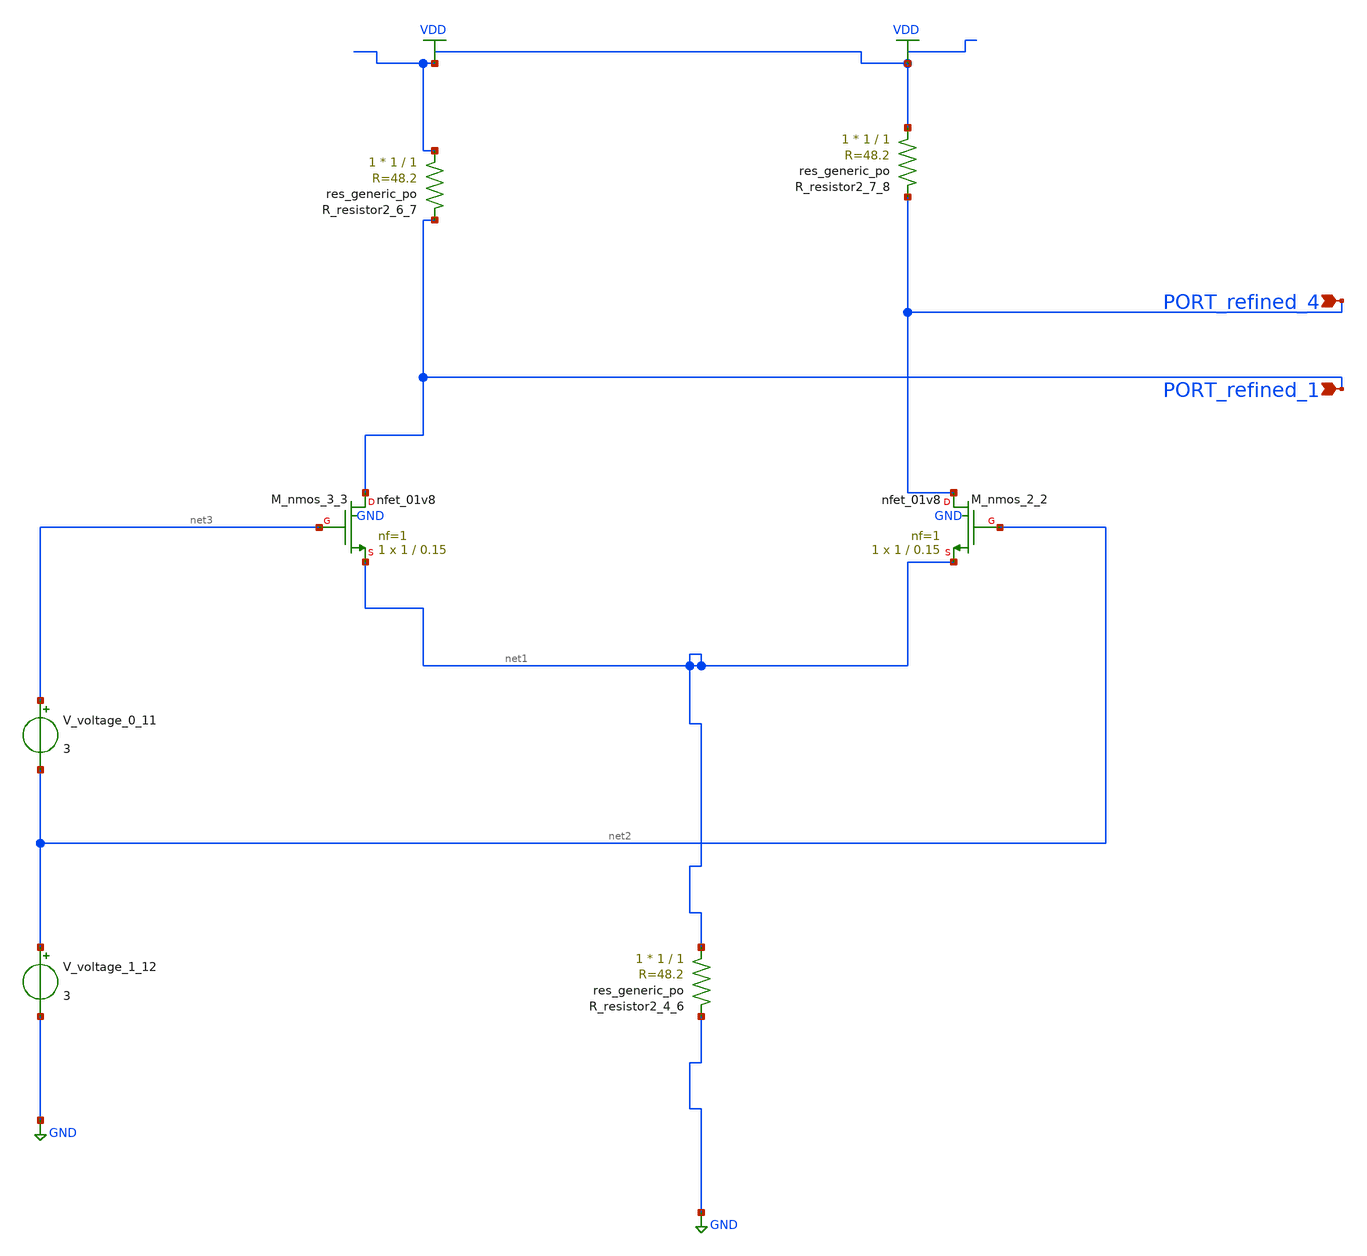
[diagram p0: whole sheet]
** sch_path: schematics/AMSNet/215.sch
**.subckt 215 PORT_refined_4 PORT_refined_1
*.ipin PORT_refined_4
*.ipin PORT_refined_1
XM_nmos_2_2 PORT_refined_4 net2 net1 GND sky130_fd_pr__nfet_01v8 L=0.15 W=1 nf=1 ad='int((1 + 1)/2) * 1 / 1 * 0.29'
+ as='int((1 + 2)/2) * 1 / 1 * 0.29' pd='2*int((1 + 1)/2) * (1 / 1 + 0.29)' ps='2*int((1 + 2)/2) * (1 / 1 + 0.29)'
+ nrd='0.29 / 1 ' nrs='0.29 / 1 ' sa=0 sb=0 sd=0 mult=1 m=1
XM_nmos_3_3 PORT_refined_1 net3 net1 GND sky130_fd_pr__nfet_01v8 L=0.15 W=1 nf=1 ad='int((1 + 1)/2) * 1 / 1 * 0.29'
+ as='int((1 + 2)/2) * 1 / 1 * 0.29' pd='2*int((1 + 1)/2) * (1 / 1 + 0.29)' ps='2*int((1 + 2)/2) * (1 / 1 + 0.29)'
+ nrd='0.29 / 1 ' nrs='0.29 / 1 ' sa=0 sb=0 sd=0 mult=1 m=1
XR_resistor2_4_6 net1 GND sky130_fd_pr__res_generic_po W=1 L=1 m=1
XR_resistor2_6_7 VDD PORT_refined_1 sky130_fd_pr__res_generic_po W=1 L=1 m=1
XR_resistor2_7_8 VDD PORT_refined_4 sky130_fd_pr__res_generic_po W=1 L=1 m=1
V_voltage_0_11 net3 net2 3
V_voltage_1_12 net2 GND 3
**.ends
.GLOBAL GND
.GLOBAL VDD
.end
